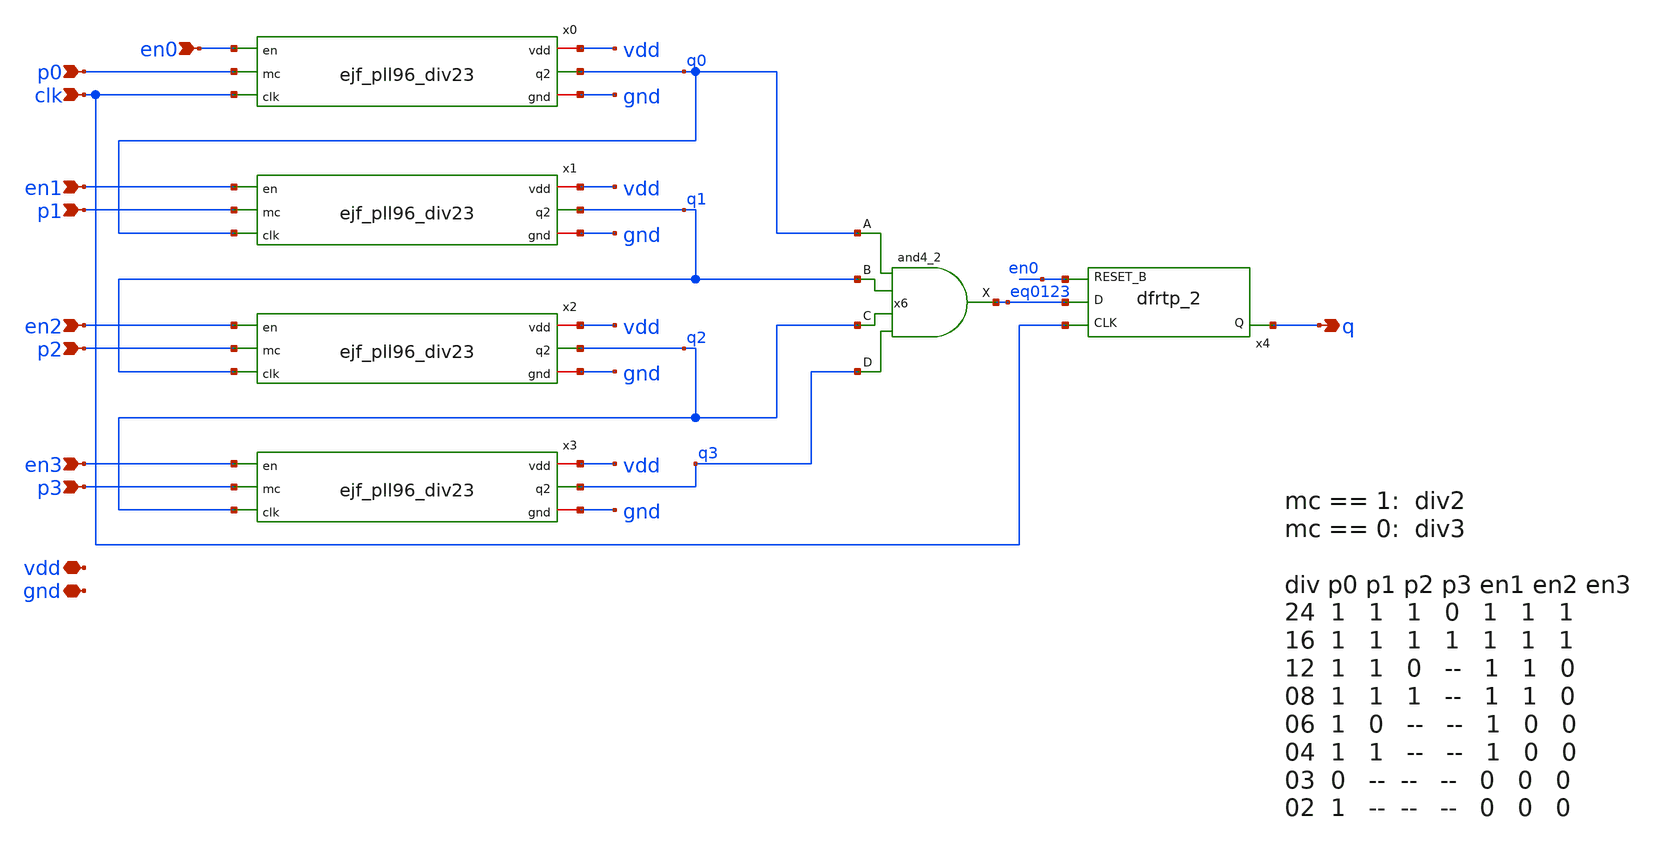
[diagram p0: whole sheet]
** sch_path: xschem/ejf_pll96_div_p.sch
**.subckt ejf_pll96_div_p vdd gnd clk p1 p2 p3 en3 en2 q en1 en0 p0
*.iopin vdd
*.iopin gnd
*.ipin clk
*.ipin p1
*.ipin p2
*.ipin p3
*.ipin en3
*.ipin en2
*.opin q
*.ipin en1
*.ipin en0
*.ipin p0
x0 q0 clk p0 vdd gnd en0 ejf_pll96_div23
x1 q1 q0 p1 vdd gnd en1 ejf_pll96_div23
x2 q2 q1 p2 vdd gnd en2 ejf_pll96_div23
x3 q3 q2 p3 vdd gnd en3 ejf_pll96_div23
x6 q0 q1 q2 q3 gnd gnd vdd vdd eq0123 sky130_fd_sc_ls__and4_2
x4 clk eq0123 en0 gnd gnd vdd vdd q sky130_fd_sc_ls__dfrtp_2
**.ends

* expanding   symbol:  ejf_pll96_div23.sym # of pins=6
** sym_path: xschem/ejf_pll96_div23.sym
** sch_path: xschem/ejf_pll96_div23.sch
.subckt ejf_pll96_div23 q2 clk mc vdd gnd en
*.ipin clk
*.ipin mc
*.opin q2
*.iopin vdd
*.iopin gnd
*.ipin en
x3 q1 mc net1 gnd gnd vdd vdd d2 sky130_fd_sc_ls__o21a_1
x1 clk net1 en gnd gnd vdd vdd q1 sky130_fd_sc_ls__dfstp_2
x2 clk d2 en gnd gnd vdd vdd q2 net1 sky130_fd_sc_ls__dfsbp_2
.ends

.end
